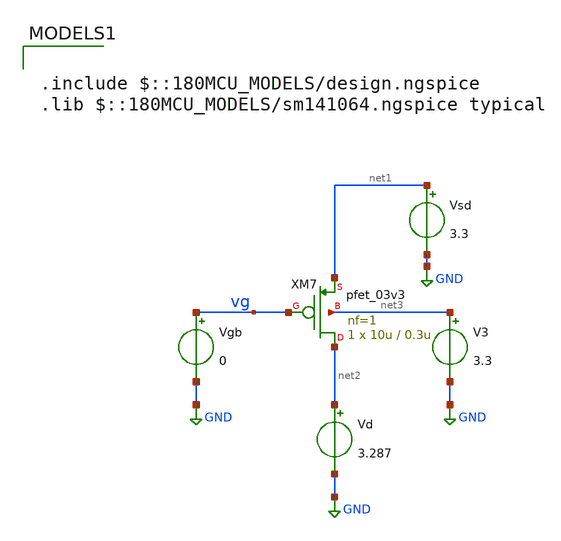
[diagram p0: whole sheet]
** sch_path: legacy/Examples/GF180MCU/xschem/Extraction/pmos_ext.sch
**.subckt pmos_ext
Vgb vg GND 0
Vsd net1 GND 3.3
V3 net3 GND 3.3
Vd net2 GND 3.287
XM7 net2 vg net1 net3 pfet_03v3 L=0.3u W=10u nf=1 ad='int((nf+1)/2) * W/nf * 0.18u' as='int((nf+2)/2) * W/nf * 0.18u'
+ pd='2*int((nf+1)/2) * (W/nf + 0.18u)' ps='2*int((nf+2)/2) * (W/nf + 0.18u)' nrd='0.18u / W' nrs='0.18u / W'
+ sa=0 sb=0 sd=0 m=1
**** begin user architecture code



.control
save all
dc Vgb 0.05 3 10m

let gm_id = -deriv(ln(i(Vd)))
save gm_id

meas dc gm_id_max MAX gm_id
let gm_id_vt = 0.531*gm_id_max
save gm_id_vt

meas dc vt FIND V(vg) WHEN gm_id=gm_id_vt
let vt0=vt-3.3
meas dc is0_ FIND i(Vd) WHEN V(vg)=vt

let is0 = is0_/0.88
let VT_val=0.026
let n = 1/(gm_id_max*VT_val)
save is0 vt0 n
echo
echo
echo

echo Extracted parameters:
print is0 vt0 n


echo
echo
echo

remzerovec
write pmos_ext.raw

.endc




.include $::180MCU_MODELS/design.ngspice
.lib $::180MCU_MODELS/sm141064.ngspice typical

**** end user architecture code
**.ends
.GLOBAL GND
.end
